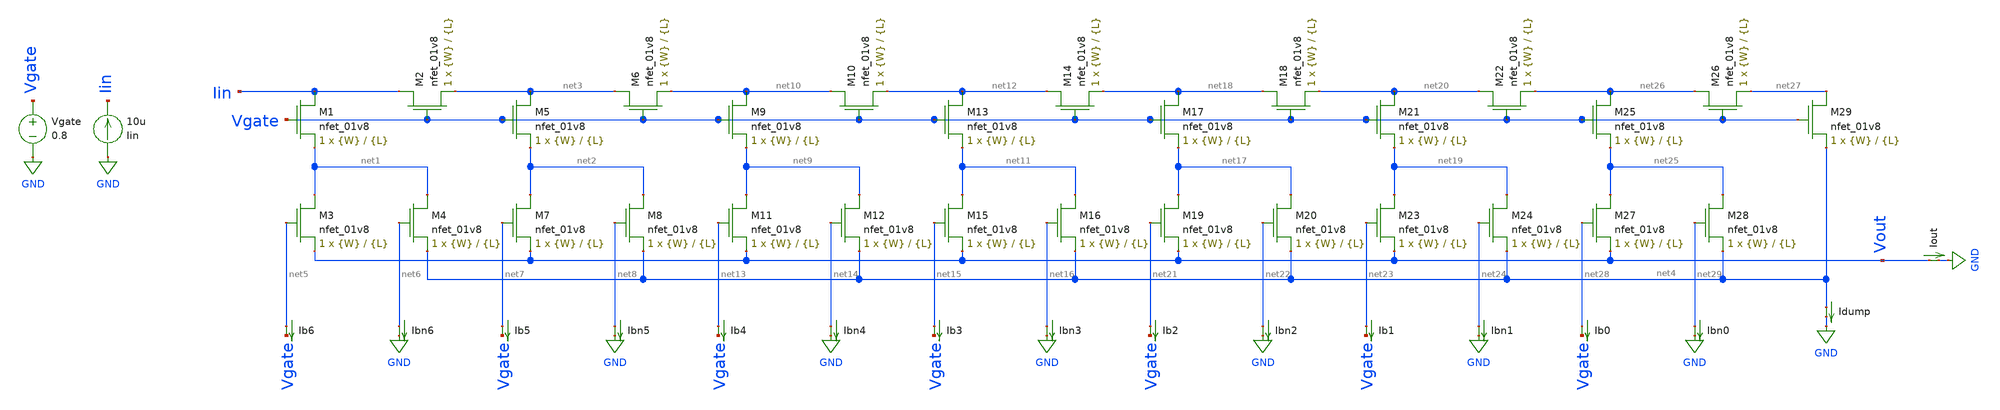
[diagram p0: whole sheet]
** sch_path: schematics/dac_from_paper.sch
**.subckt dac_from_paper
XM1 Iin Vgate net1 GND sky130_fd_pr__nfet_01v8 L={L} W={W} nf=1 ad='int((nf+1)/2) * W/nf * 0.29' as='int((nf+2)/2) * W/nf * 0.29'
+ pd='2*int((nf+1)/2) * (W/nf + 0.29)' ps='2*int((nf+2)/2) * (W/nf + 0.29)' nrd='0.29 / W' nrs='0.29 / W'
+ sa=0 sb=0 sd=0 mult=1 m=1
XM2 Iin Vgate net3 GND sky130_fd_pr__nfet_01v8 L={L} W={W} nf=1 ad='int((nf+1)/2) * W/nf * 0.29' as='int((nf+2)/2) * W/nf * 0.29'
+ pd='2*int((nf+1)/2) * (W/nf + 0.29)' ps='2*int((nf+2)/2) * (W/nf + 0.29)' nrd='0.29 / W' nrs='0.29 / W'
+ sa=0 sb=0 sd=0 mult=1 m=1
XM3 net1 net5 Vout GND sky130_fd_pr__nfet_01v8 L={L} W={W} nf=1 ad='int((nf+1)/2) * W/nf * 0.29' as='int((nf+2)/2) * W/nf * 0.29'
+ pd='2*int((nf+1)/2) * (W/nf + 0.29)' ps='2*int((nf+2)/2) * (W/nf + 0.29)' nrd='0.29 / W' nrs='0.29 / W'
+ sa=0 sb=0 sd=0 mult=1 m=1
XM4 net1 net6 net4 GND sky130_fd_pr__nfet_01v8 L={L} W={W} nf=1 ad='int((nf+1)/2) * W/nf * 0.29' as='int((nf+2)/2) * W/nf * 0.29'
+ pd='2*int((nf+1)/2) * (W/nf + 0.29)' ps='2*int((nf+2)/2) * (W/nf + 0.29)' nrd='0.29 / W' nrs='0.29 / W'
+ sa=0 sb=0 sd=0 mult=1 m=1
XM5 net3 Vgate net2 GND sky130_fd_pr__nfet_01v8 L={L} W={W} nf=1 ad='int((nf+1)/2) * W/nf * 0.29' as='int((nf+2)/2) * W/nf * 0.29'
+ pd='2*int((nf+1)/2) * (W/nf + 0.29)' ps='2*int((nf+2)/2) * (W/nf + 0.29)' nrd='0.29 / W' nrs='0.29 / W'
+ sa=0 sb=0 sd=0 mult=1 m=1
XM6 net3 Vgate net10 GND sky130_fd_pr__nfet_01v8 L={L} W={W} nf=1 ad='int((nf+1)/2) * W/nf * 0.29' as='int((nf+2)/2) * W/nf * 0.29'
+ pd='2*int((nf+1)/2) * (W/nf + 0.29)' ps='2*int((nf+2)/2) * (W/nf + 0.29)' nrd='0.29 / W' nrs='0.29 / W'
+ sa=0 sb=0 sd=0 mult=1 m=1
XM7 net2 net7 Vout GND sky130_fd_pr__nfet_01v8 L={L} W={W} nf=1 ad='int((nf+1)/2) * W/nf * 0.29' as='int((nf+2)/2) * W/nf * 0.29'
+ pd='2*int((nf+1)/2) * (W/nf + 0.29)' ps='2*int((nf+2)/2) * (W/nf + 0.29)' nrd='0.29 / W' nrs='0.29 / W'
+ sa=0 sb=0 sd=0 mult=1 m=1
XM8 net2 net8 net4 GND sky130_fd_pr__nfet_01v8 L={L} W={W} nf=1 ad='int((nf+1)/2) * W/nf * 0.29' as='int((nf+2)/2) * W/nf * 0.29'
+ pd='2*int((nf+1)/2) * (W/nf + 0.29)' ps='2*int((nf+2)/2) * (W/nf + 0.29)' nrd='0.29 / W' nrs='0.29 / W'
+ sa=0 sb=0 sd=0 mult=1 m=1
XM9 net10 Vgate net9 GND sky130_fd_pr__nfet_01v8 L={L} W={W} nf=1 ad='int((nf+1)/2) * W/nf * 0.29' as='int((nf+2)/2) * W/nf * 0.29'
+ pd='2*int((nf+1)/2) * (W/nf + 0.29)' ps='2*int((nf+2)/2) * (W/nf + 0.29)' nrd='0.29 / W' nrs='0.29 / W'
+ sa=0 sb=0 sd=0 mult=1 m=1
XM10 net10 Vgate net12 GND sky130_fd_pr__nfet_01v8 L={L} W={W} nf=1 ad='int((nf+1)/2) * W/nf * 0.29'
+ as='int((nf+2)/2) * W/nf * 0.29' pd='2*int((nf+1)/2) * (W/nf + 0.29)' ps='2*int((nf+2)/2) * (W/nf + 0.29)'
+ nrd='0.29 / W' nrs='0.29 / W' sa=0 sb=0 sd=0 mult=1 m=1
XM11 net9 net13 Vout GND sky130_fd_pr__nfet_01v8 L={L} W={W} nf=1 ad='int((nf+1)/2) * W/nf * 0.29' as='int((nf+2)/2) * W/nf * 0.29'
+ pd='2*int((nf+1)/2) * (W/nf + 0.29)' ps='2*int((nf+2)/2) * (W/nf + 0.29)' nrd='0.29 / W' nrs='0.29 / W'
+ sa=0 sb=0 sd=0 mult=1 m=1
XM12 net9 net14 net4 GND sky130_fd_pr__nfet_01v8 L={L} W={W} nf=1 ad='int((nf+1)/2) * W/nf * 0.29' as='int((nf+2)/2) * W/nf * 0.29'
+ pd='2*int((nf+1)/2) * (W/nf + 0.29)' ps='2*int((nf+2)/2) * (W/nf + 0.29)' nrd='0.29 / W' nrs='0.29 / W'
+ sa=0 sb=0 sd=0 mult=1 m=1
XM13 net12 Vgate net11 GND sky130_fd_pr__nfet_01v8 L={L} W={W} nf=1 ad='int((nf+1)/2) * W/nf * 0.29'
+ as='int((nf+2)/2) * W/nf * 0.29' pd='2*int((nf+1)/2) * (W/nf + 0.29)' ps='2*int((nf+2)/2) * (W/nf + 0.29)'
+ nrd='0.29 / W' nrs='0.29 / W' sa=0 sb=0 sd=0 mult=1 m=1
XM14 net12 Vgate net18 GND sky130_fd_pr__nfet_01v8 L={L} W={W} nf=1 ad='int((nf+1)/2) * W/nf * 0.29'
+ as='int((nf+2)/2) * W/nf * 0.29' pd='2*int((nf+1)/2) * (W/nf + 0.29)' ps='2*int((nf+2)/2) * (W/nf + 0.29)'
+ nrd='0.29 / W' nrs='0.29 / W' sa=0 sb=0 sd=0 mult=1 m=1
XM15 net11 net15 Vout GND sky130_fd_pr__nfet_01v8 L={L} W={W} nf=1 ad='int((nf+1)/2) * W/nf * 0.29' as='int((nf+2)/2) * W/nf * 0.29'
+ pd='2*int((nf+1)/2) * (W/nf + 0.29)' ps='2*int((nf+2)/2) * (W/nf + 0.29)' nrd='0.29 / W' nrs='0.29 / W'
+ sa=0 sb=0 sd=0 mult=1 m=1
XM16 net11 net16 net4 GND sky130_fd_pr__nfet_01v8 L={L} W={W} nf=1 ad='int((nf+1)/2) * W/nf * 0.29' as='int((nf+2)/2) * W/nf * 0.29'
+ pd='2*int((nf+1)/2) * (W/nf + 0.29)' ps='2*int((nf+2)/2) * (W/nf + 0.29)' nrd='0.29 / W' nrs='0.29 / W'
+ sa=0 sb=0 sd=0 mult=1 m=1
XM17 net18 Vgate net17 GND sky130_fd_pr__nfet_01v8 L={L} W={W} nf=1 ad='int((nf+1)/2) * W/nf * 0.29'
+ as='int((nf+2)/2) * W/nf * 0.29' pd='2*int((nf+1)/2) * (W/nf + 0.29)' ps='2*int((nf+2)/2) * (W/nf + 0.29)'
+ nrd='0.29 / W' nrs='0.29 / W' sa=0 sb=0 sd=0 mult=1 m=1
XM18 net18 Vgate net20 GND sky130_fd_pr__nfet_01v8 L={L} W={W} nf=1 ad='int((nf+1)/2) * W/nf * 0.29'
+ as='int((nf+2)/2) * W/nf * 0.29' pd='2*int((nf+1)/2) * (W/nf + 0.29)' ps='2*int((nf+2)/2) * (W/nf + 0.29)'
+ nrd='0.29 / W' nrs='0.29 / W' sa=0 sb=0 sd=0 mult=1 m=1
XM19 net17 net21 Vout GND sky130_fd_pr__nfet_01v8 L={L} W={W} nf=1 ad='int((nf+1)/2) * W/nf * 0.29' as='int((nf+2)/2) * W/nf * 0.29'
+ pd='2*int((nf+1)/2) * (W/nf + 0.29)' ps='2*int((nf+2)/2) * (W/nf + 0.29)' nrd='0.29 / W' nrs='0.29 / W'
+ sa=0 sb=0 sd=0 mult=1 m=1
XM20 net17 net22 net4 GND sky130_fd_pr__nfet_01v8 L={L} W={W} nf=1 ad='int((nf+1)/2) * W/nf * 0.29' as='int((nf+2)/2) * W/nf * 0.29'
+ pd='2*int((nf+1)/2) * (W/nf + 0.29)' ps='2*int((nf+2)/2) * (W/nf + 0.29)' nrd='0.29 / W' nrs='0.29 / W'
+ sa=0 sb=0 sd=0 mult=1 m=1
XM21 net20 Vgate net19 GND sky130_fd_pr__nfet_01v8 L={L} W={W} nf=1 ad='int((nf+1)/2) * W/nf * 0.29'
+ as='int((nf+2)/2) * W/nf * 0.29' pd='2*int((nf+1)/2) * (W/nf + 0.29)' ps='2*int((nf+2)/2) * (W/nf + 0.29)'
+ nrd='0.29 / W' nrs='0.29 / W' sa=0 sb=0 sd=0 mult=1 m=1
XM22 net20 Vgate net26 GND sky130_fd_pr__nfet_01v8 L={L} W={W} nf=1 ad='int((nf+1)/2) * W/nf * 0.29'
+ as='int((nf+2)/2) * W/nf * 0.29' pd='2*int((nf+1)/2) * (W/nf + 0.29)' ps='2*int((nf+2)/2) * (W/nf + 0.29)'
+ nrd='0.29 / W' nrs='0.29 / W' sa=0 sb=0 sd=0 mult=1 m=1
XM23 net19 net23 Vout GND sky130_fd_pr__nfet_01v8 L={L} W={W} nf=1 ad='int((nf+1)/2) * W/nf * 0.29' as='int((nf+2)/2) * W/nf * 0.29'
+ pd='2*int((nf+1)/2) * (W/nf + 0.29)' ps='2*int((nf+2)/2) * (W/nf + 0.29)' nrd='0.29 / W' nrs='0.29 / W'
+ sa=0 sb=0 sd=0 mult=1 m=1
XM24 net19 net24 net4 GND sky130_fd_pr__nfet_01v8 L={L} W={W} nf=1 ad='int((nf+1)/2) * W/nf * 0.29' as='int((nf+2)/2) * W/nf * 0.29'
+ pd='2*int((nf+1)/2) * (W/nf + 0.29)' ps='2*int((nf+2)/2) * (W/nf + 0.29)' nrd='0.29 / W' nrs='0.29 / W'
+ sa=0 sb=0 sd=0 mult=1 m=1
XM25 net26 Vgate net25 GND sky130_fd_pr__nfet_01v8 L={L} W={W} nf=1 ad='int((nf+1)/2) * W/nf * 0.29'
+ as='int((nf+2)/2) * W/nf * 0.29' pd='2*int((nf+1)/2) * (W/nf + 0.29)' ps='2*int((nf+2)/2) * (W/nf + 0.29)'
+ nrd='0.29 / W' nrs='0.29 / W' sa=0 sb=0 sd=0 mult=1 m=1
XM26 net26 Vgate net27 GND sky130_fd_pr__nfet_01v8 L={L} W={W} nf=1 ad='int((nf+1)/2) * W/nf * 0.29'
+ as='int((nf+2)/2) * W/nf * 0.29' pd='2*int((nf+1)/2) * (W/nf + 0.29)' ps='2*int((nf+2)/2) * (W/nf + 0.29)'
+ nrd='0.29 / W' nrs='0.29 / W' sa=0 sb=0 sd=0 mult=1 m=1
XM27 net25 net28 Vout GND sky130_fd_pr__nfet_01v8 L={L} W={W} nf=1 ad='int((nf+1)/2) * W/nf * 0.29' as='int((nf+2)/2) * W/nf * 0.29'
+ pd='2*int((nf+1)/2) * (W/nf + 0.29)' ps='2*int((nf+2)/2) * (W/nf + 0.29)' nrd='0.29 / W' nrs='0.29 / W'
+ sa=0 sb=0 sd=0 mult=1 m=1
XM28 net25 net29 net4 GND sky130_fd_pr__nfet_01v8 L={L} W={W} nf=1 ad='int((nf+1)/2) * W/nf * 0.29' as='int((nf+2)/2) * W/nf * 0.29'
+ pd='2*int((nf+1)/2) * (W/nf + 0.29)' ps='2*int((nf+2)/2) * (W/nf + 0.29)' nrd='0.29 / W' nrs='0.29 / W'
+ sa=0 sb=0 sd=0 mult=1 m=1
XM29 net27 Vgate net4 GND sky130_fd_pr__nfet_01v8 L={L} W={W} nf=1 ad='int((nf+1)/2) * W/nf * 0.29' as='int((nf+2)/2) * W/nf * 0.29'
+ pd='2*int((nf+1)/2) * (W/nf + 0.29)' ps='2*int((nf+2)/2) * (W/nf + 0.29)' nrd='0.29 / W' nrs='0.29 / W'
+ sa=0 sb=0 sd=0 mult=1 m=1
Idump net4 GND 0
.save i(idump)
Iout Vout GND 0
.save i(iout)
Vgate Vgate GND 0.8
Ib0 net28 Vgate 0
.save i(ib0)
Ib1 net23 Vgate 0
.save i(ib1)
Ib2 net21 Vgate 0
.save i(ib2)
Ib3 net15 Vgate 0
.save i(ib3)
Ib4 net13 Vgate 0
.save i(ib4)
Ib5 net7 Vgate 0
.save i(ib5)
Ib6 net5 Vgate 0
.save i(ib6)
Ibn0 net29 GND 0
.save i(ibn0)
Ibn1 net24 GND 0
.save i(ibn1)
Ibn2 net22 GND 0
.save i(ibn2)
Ibn3 net16 GND 0
.save i(ibn3)
Ibn4 net14 GND 0
.save i(ibn4)
Ibn5 net8 GND 0
.save i(ibn5)
Ibn6 net6 GND 0
.save i(ibn6)
Iin GND Iin 10u
**** begin user architecture code

.option wnflag=1
.param MC_SWITCH=0.0
.lib ~/skywater/skywater-pdk/libraries/sky130_fd_pr_ngspice/latest/models/sky130.lib.spice tt


.param W=1
.param L=0.5
.tran 1u 100u
.save all

**** end user architecture code
**.ends
.GLOBAL GND
.end
